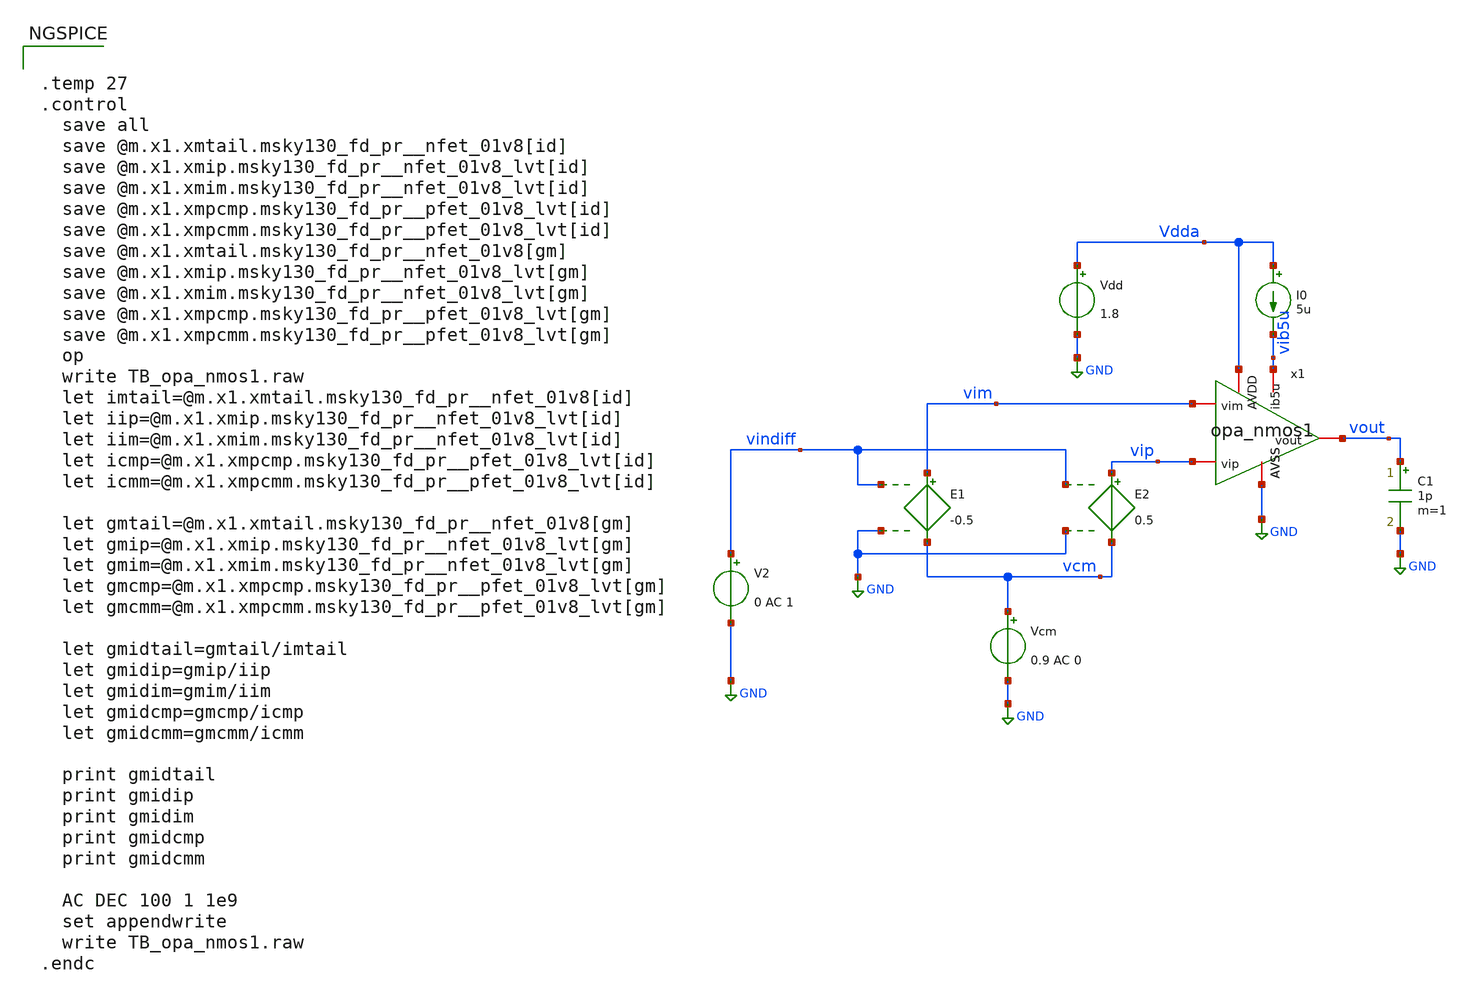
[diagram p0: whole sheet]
** sch_path: xschem/TB_opa_nmos1.sch
**.subckt TB_opa_nmos1
x1 vout vip vim GND Vdda vib5u opa_nmos1
Vcm vcm GND 0.9 AC 0
E1 vim vcm vindiff GND -0.5
E2 vip vcm vindiff GND 0.5
V2 vindiff GND 0 AC 1
I0 Vdda vib5u 5u
Vdd Vdda GND 1.8
C1 vout GND 1p m=1
**** begin user architecture code

** opencircuitdesign pdks install
.lib $::SKYWATER_MODELS/sky130.lib.spice tt



.temp 27
.control
  save all
  save @m.x1.xmtail.msky130_fd_pr__nfet_01v8[id]
  save @m.x1.xmip.msky130_fd_pr__nfet_01v8_lvt[id]
  save @m.x1.xmim.msky130_fd_pr__nfet_01v8_lvt[id]
  save @m.x1.xmpcmp.msky130_fd_pr__pfet_01v8_lvt[id]
  save @m.x1.xmpcmm.msky130_fd_pr__pfet_01v8_lvt[id]
  save @m.x1.xmtail.msky130_fd_pr__nfet_01v8[gm]
  save @m.x1.xmip.msky130_fd_pr__nfet_01v8_lvt[gm]
  save @m.x1.xmim.msky130_fd_pr__nfet_01v8_lvt[gm]
  save @m.x1.xmpcmp.msky130_fd_pr__pfet_01v8_lvt[gm]
  save @m.x1.xmpcmm.msky130_fd_pr__pfet_01v8_lvt[gm]
  op
  write TB_opa_nmos1.raw
  let imtail=@m.x1.xmtail.msky130_fd_pr__nfet_01v8[id]
  let iip=@m.x1.xmip.msky130_fd_pr__nfet_01v8_lvt[id]
  let iim=@m.x1.xmim.msky130_fd_pr__nfet_01v8_lvt[id]
  let icmp=@m.x1.xmpcmp.msky130_fd_pr__pfet_01v8_lvt[id]
  let icmm=@m.x1.xmpcmm.msky130_fd_pr__pfet_01v8_lvt[id]

  let gmtail=@m.x1.xmtail.msky130_fd_pr__nfet_01v8[gm]
  let gmip=@m.x1.xmip.msky130_fd_pr__nfet_01v8_lvt[gm]
  let gmim=@m.x1.xmim.msky130_fd_pr__nfet_01v8_lvt[gm]
  let gmcmp=@m.x1.xmpcmp.msky130_fd_pr__pfet_01v8_lvt[gm]
  let gmcmm=@m.x1.xmpcmm.msky130_fd_pr__pfet_01v8_lvt[gm]

  let gmidtail=gmtail/imtail
  let gmidip=gmip/iip
  let gmidim=gmim/iim
  let gmidcmp=gmcmp/icmp
  let gmidcmm=gmcmm/icmm

  print gmidtail
  print gmidip
  print gmidim
  print gmidcmp
  print gmidcmm

  AC DEC 100 1 1e9
  set appendwrite
  write TB_opa_nmos1.raw
.endc


**** end user architecture code
**.ends

* expanding   symbol:  opa_nmos1.sym # of pins=6
** sym_path: xschem/opa_nmos1.sym
** sch_path: xschem/opa_nmos1.sch
.subckt opa_nmos1 vout vip vim AVSS AVDD ib5u
*.iopin vip
*.iopin vim
*.iopin AVDD
*.iopin AVSS
*.iopin ib5u
*.iopin vout
XMtail vs ib5u AVSS AVSS sky130_fd_pr__nfet_01v8 L=1 W=5 nf=1 ad='int((1 + 1)/2) * 5 / 1 * 0.29' as='int((1 + 2)/2) * 5 / 1 * 0.29'
+ pd='2*int((1 + 1)/2) * (5 / 1 + 0.29)' ps='2*int((1 + 2)/2) * (5 / 1 + 0.29)' nrd='0.29 / 5 ' nrs='0.29 / 5 '
+ sa=0 sb=0 sd=0 mult=2 m=2
XM1 ib5u ib5u AVSS AVSS sky130_fd_pr__nfet_01v8 L=1 W=5 nf=1 ad='int((1 + 1)/2) * 5 / 1 * 0.29' as='int((1 + 2)/2) * 5 / 1 * 0.29'
+ pd='2*int((1 + 1)/2) * (5 / 1 + 0.29)' ps='2*int((1 + 2)/2) * (5 / 1 + 0.29)' nrd='0.29 / 5 ' nrs='0.29 / 5 '
+ sa=0 sb=0 sd=0 mult=1 m=1
XMip vom vip vs vs sky130_fd_pr__nfet_01v8_lvt L=2 W=5 nf=1 ad='int((1 + 1)/2) * 5 / 1 * 0.29' as='int((1 + 2)/2) * 5 / 1 * 0.29'
+ pd='2*int((1 + 1)/2) * (5 / 1 + 0.29)' ps='2*int((1 + 2)/2) * (5 / 1 + 0.29)' nrd='0.29 / 5 ' nrs='0.29 / 5 '
+ sa=0 sb=0 sd=0 mult=4 m=4
XMim vout vim vs vs sky130_fd_pr__nfet_01v8_lvt L=2 W=5 nf=1 ad='int((1 + 1)/2) * 5 / 1 * 0.29' as='int((1 + 2)/2) * 5 / 1 * 0.29'
+ pd='2*int((1 + 1)/2) * (5 / 1 + 0.29)' ps='2*int((1 + 2)/2) * (5 / 1 + 0.29)' nrd='0.29 / 5 ' nrs='0.29 / 5 '
+ sa=0 sb=0 sd=0 mult=4 m=4
XMpcmm vout vom AVDD AVDD sky130_fd_pr__pfet_01v8_lvt L=2 W=5 nf=1 ad='int((1 + 1)/2) * 5 / 1 * 0.29'
+ as='int((1 + 2)/2) * 5 / 1 * 0.29' pd='2*int((1 + 1)/2) * (5 / 1 + 0.29)' ps='2*int((1 + 2)/2) * (5 / 1 + 0.29)'
+ nrd='0.29 / 5 ' nrs='0.29 / 5 ' sa=0 sb=0 sd=0 mult=2 m=2
XMpcmp vom vom AVDD AVDD sky130_fd_pr__pfet_01v8_lvt L=2 W=5 nf=1 ad='int((1 + 1)/2) * 5 / 1 * 0.29'
+ as='int((1 + 2)/2) * 5 / 1 * 0.29' pd='2*int((1 + 1)/2) * (5 / 1 + 0.29)' ps='2*int((1 + 2)/2) * (5 / 1 + 0.29)'
+ nrd='0.29 / 5 ' nrs='0.29 / 5 ' sa=0 sb=0 sd=0 mult=2 m=2
.ends

.GLOBAL GND
.end
